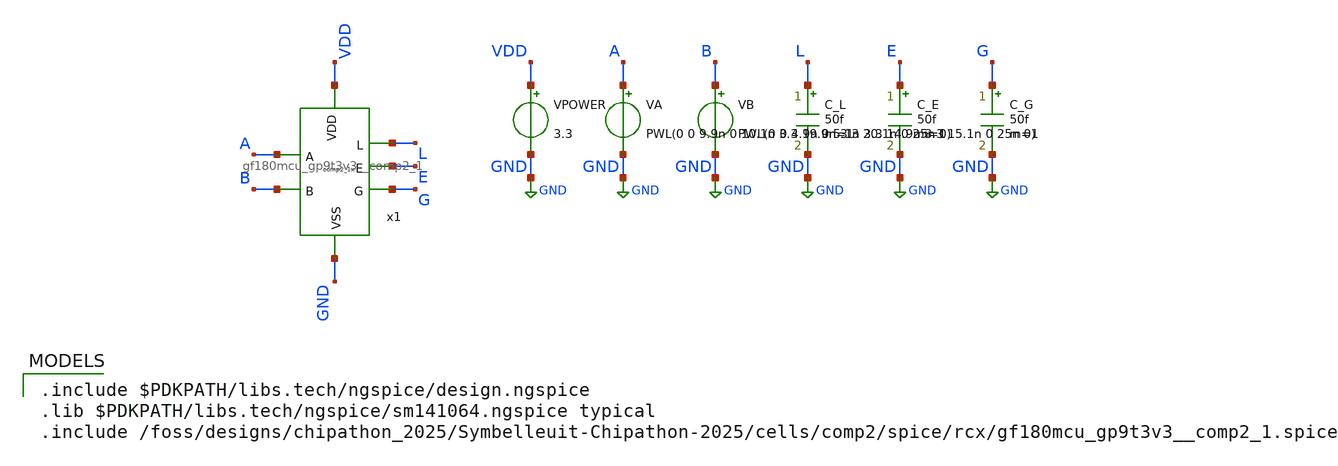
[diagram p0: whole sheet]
** sch_path: cells/comp2/cace/templates/comp2_tb_func.sch
**.subckt comp2_tb_func
x1 VDD L A E G B GND gf180mcu_gp9t3v3__comp2_1
VPOWER VDD GND 3.3
VA A GND PWL(0 0 9.9n 0 10.1n 3.3 19.9n 3.3 20.1n 0 25n 0)
VB B GND PWL(0 0 4.9n 0 5.1n 3.3 14.9n 3.3 15.1n 0 25n 0)
C_L L GND 50f m=1
C_E E GND 50f m=1
C_G G GND 50f m=1
**** begin user architecture code

.include $PDKPATH/libs.tech/ngspice/design.ngspice
.lib $PDKPATH/libs.tech/ngspice/sm141064.ngspice typical
.include /foss/designs/chipathon_2025/Symbelleuit-Chipathon-2025/cells/comp2/spice/rcx/gf180mcu_gp9t3v3__comp2_1.spice


* CACE Functional Truth-Table Error Simulation
.tran 100p 25n
.control
  run
  * State 00: A=0, B=0 -> L=0, E=3.3, G=0
  meas tran v_L_00 FIND v(L) AT=2.5n
  meas tran v_E_00 FIND v(E) AT=2.5n
  meas tran v_G_00 FIND v(G) AT=2.5n

  * State 01: A=0, B=1 -> L=3.3, E=0, G=0
  meas tran v_L_01 FIND v(L) AT=7.5n
  meas tran v_E_01 FIND v(E) AT=7.5n
  meas tran v_G_01 FIND v(G) AT=7.5n

  * State 11: A=1, B=1 -> L=0, E=3.3, G=0
  meas tran v_L_11 FIND v(L) AT=12.5n
  meas tran v_E_11 FIND v(E) AT=12.5n
  meas tran v_G_11 FIND v(G) AT=12.5n

  * State 10: A=1, B=0 -> L=0, E=0, G=3.3
  meas tran v_L_10 FIND v(L) AT=17.5n
  meas tran v_E_10 FIND v(E) AT=17.5n
  meas tran v_G_10 FIND v(G) AT=17.5n

  let err_00 = v_L_00 + abs(v_E_00 - 3.3) + v_G_00
  let err_01 = abs(v_L_01 - 3.3) + v_E_01 + v_G_01
  let err_11 = v_L_11 + abs(v_E_11 - 3.3) + v_G_11
  let err_10 = v_L_10 + v_E_10 + abs(v_G_10 - 3.3)
  let func_total_err = err_00 + err_01 + err_11 + err_10
  print func_total_err
  echo $&func_total_err > comp2_tb_func_0.data
.endc
.GLOBAL GND


**** end user architecture code
**.ends
.GLOBAL GND
.end
